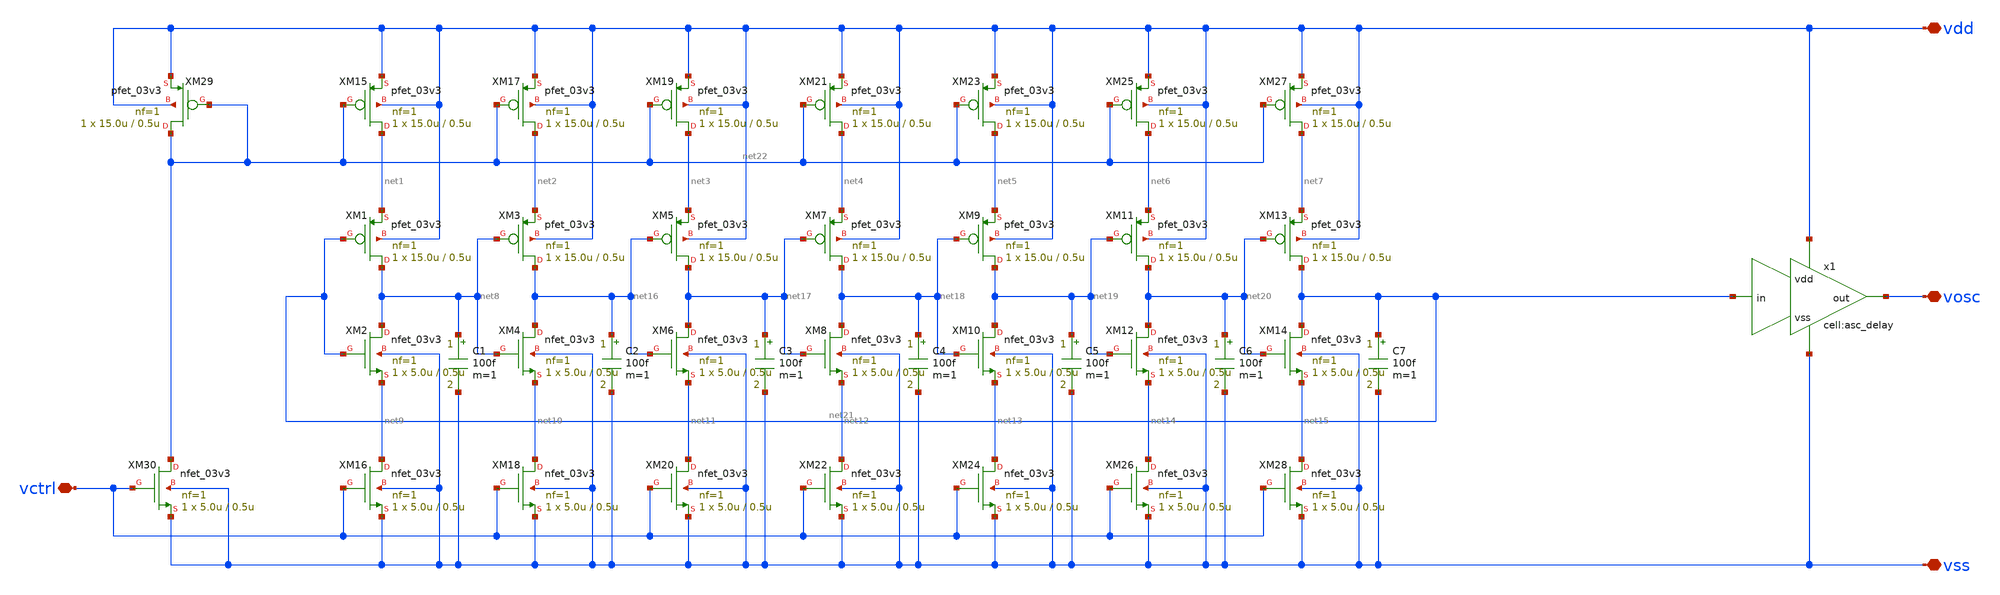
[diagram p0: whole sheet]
** sch_path: designs/libs/core_analog/CSRVCO_20250821/CSRVCO_20250821.sch
**.subckt CSRVCO_20250821 vdd vss vosc vctrl
*.iopin vdd
*.iopin vss
*.iopin vosc
*.iopin vctrl
XM1 net8 net21 net1 vdd pfet_03v3 L=0.5u W=15.0u nf=1 ad='int((nf+1)/2) * W/nf * 0.18u' as='int((nf+2)/2) * W/nf * 0.18u'
+ pd='2*int((nf+1)/2) * (W/nf + 0.18u)' ps='2*int((nf+2)/2) * (W/nf + 0.18u)' nrd='0.18u / W' nrs='0.18u / W'
+ sa=0 sb=0 sd=0 m=1
XM2 net8 net21 net9 vss nfet_03v3 L=0.5u W=5.0u nf=1 ad='int((nf+1)/2) * W/nf * 0.18u' as='int((nf+2)/2) * W/nf * 0.18u'
+ pd='2*int((nf+1)/2) * (W/nf + 0.18u)' ps='2*int((nf+2)/2) * (W/nf + 0.18u)' nrd='0.18u / W' nrs='0.18u / W'
+ sa=0 sb=0 sd=0 m=1
XM3 net16 net8 net2 vdd pfet_03v3 L=0.5u W=15.0u nf=1 ad='int((nf+1)/2) * W/nf * 0.18u' as='int((nf+2)/2) * W/nf * 0.18u'
+ pd='2*int((nf+1)/2) * (W/nf + 0.18u)' ps='2*int((nf+2)/2) * (W/nf + 0.18u)' nrd='0.18u / W' nrs='0.18u / W'
+ sa=0 sb=0 sd=0 m=1
XM4 net16 net8 net10 vss nfet_03v3 L=0.5u W=5.0u nf=1 ad='int((nf+1)/2) * W/nf * 0.18u' as='int((nf+2)/2) * W/nf * 0.18u'
+ pd='2*int((nf+1)/2) * (W/nf + 0.18u)' ps='2*int((nf+2)/2) * (W/nf + 0.18u)' nrd='0.18u / W' nrs='0.18u / W'
+ sa=0 sb=0 sd=0 m=1
XM5 net17 net16 net3 vdd pfet_03v3 L=0.5u W=15.0u nf=1 ad='int((nf+1)/2) * W/nf * 0.18u' as='int((nf+2)/2) * W/nf * 0.18u'
+ pd='2*int((nf+1)/2) * (W/nf + 0.18u)' ps='2*int((nf+2)/2) * (W/nf + 0.18u)' nrd='0.18u / W' nrs='0.18u / W'
+ sa=0 sb=0 sd=0 m=1
XM6 net17 net16 net11 vss nfet_03v3 L=0.5u W=5.0u nf=1 ad='int((nf+1)/2) * W/nf * 0.18u' as='int((nf+2)/2) * W/nf * 0.18u'
+ pd='2*int((nf+1)/2) * (W/nf + 0.18u)' ps='2*int((nf+2)/2) * (W/nf + 0.18u)' nrd='0.18u / W' nrs='0.18u / W'
+ sa=0 sb=0 sd=0 m=1
XM7 net18 net17 net4 vdd pfet_03v3 L=0.5u W=15.0u nf=1 ad='int((nf+1)/2) * W/nf * 0.18u' as='int((nf+2)/2) * W/nf * 0.18u'
+ pd='2*int((nf+1)/2) * (W/nf + 0.18u)' ps='2*int((nf+2)/2) * (W/nf + 0.18u)' nrd='0.18u / W' nrs='0.18u / W'
+ sa=0 sb=0 sd=0 m=1
XM8 net18 net17 net12 vss nfet_03v3 L=0.5u W=5.0u nf=1 ad='int((nf+1)/2) * W/nf * 0.18u' as='int((nf+2)/2) * W/nf * 0.18u'
+ pd='2*int((nf+1)/2) * (W/nf + 0.18u)' ps='2*int((nf+2)/2) * (W/nf + 0.18u)' nrd='0.18u / W' nrs='0.18u / W'
+ sa=0 sb=0 sd=0 m=1
XM9 net19 net18 net5 vdd pfet_03v3 L=0.5u W=15.0u nf=1 ad='int((nf+1)/2) * W/nf * 0.18u' as='int((nf+2)/2) * W/nf * 0.18u'
+ pd='2*int((nf+1)/2) * (W/nf + 0.18u)' ps='2*int((nf+2)/2) * (W/nf + 0.18u)' nrd='0.18u / W' nrs='0.18u / W'
+ sa=0 sb=0 sd=0 m=1
XM10 net19 net18 net13 vss nfet_03v3 L=0.5u W=5.0u nf=1 ad='int((nf+1)/2) * W/nf * 0.18u' as='int((nf+2)/2) * W/nf * 0.18u'
+ pd='2*int((nf+1)/2) * (W/nf + 0.18u)' ps='2*int((nf+2)/2) * (W/nf + 0.18u)' nrd='0.18u / W' nrs='0.18u / W'
+ sa=0 sb=0 sd=0 m=1
XM11 net20 net19 net6 vdd pfet_03v3 L=0.5u W=15.0u nf=1 ad='int((nf+1)/2) * W/nf * 0.18u' as='int((nf+2)/2) * W/nf * 0.18u'
+ pd='2*int((nf+1)/2) * (W/nf + 0.18u)' ps='2*int((nf+2)/2) * (W/nf + 0.18u)' nrd='0.18u / W' nrs='0.18u / W'
+ sa=0 sb=0 sd=0 m=1
XM12 net20 net19 net14 vss nfet_03v3 L=0.5u W=5.0u nf=1 ad='int((nf+1)/2) * W/nf * 0.18u' as='int((nf+2)/2) * W/nf * 0.18u'
+ pd='2*int((nf+1)/2) * (W/nf + 0.18u)' ps='2*int((nf+2)/2) * (W/nf + 0.18u)' nrd='0.18u / W' nrs='0.18u / W'
+ sa=0 sb=0 sd=0 m=1
XM13 net21 net20 net7 vdd pfet_03v3 L=0.5u W=15.0u nf=1 ad='int((nf+1)/2) * W/nf * 0.18u' as='int((nf+2)/2) * W/nf * 0.18u'
+ pd='2*int((nf+1)/2) * (W/nf + 0.18u)' ps='2*int((nf+2)/2) * (W/nf + 0.18u)' nrd='0.18u / W' nrs='0.18u / W'
+ sa=0 sb=0 sd=0 m=1
XM14 net21 net20 net15 vss nfet_03v3 L=0.5u W=5.0u nf=1 ad='int((nf+1)/2) * W/nf * 0.18u' as='int((nf+2)/2) * W/nf * 0.18u'
+ pd='2*int((nf+1)/2) * (W/nf + 0.18u)' ps='2*int((nf+2)/2) * (W/nf + 0.18u)' nrd='0.18u / W' nrs='0.18u / W'
+ sa=0 sb=0 sd=0 m=1
XM15 net1 net22 vdd vdd pfet_03v3 L=0.5u W=15.0u nf=1 ad='int((nf+1)/2) * W/nf * 0.18u' as='int((nf+2)/2) * W/nf * 0.18u'
+ pd='2*int((nf+1)/2) * (W/nf + 0.18u)' ps='2*int((nf+2)/2) * (W/nf + 0.18u)' nrd='0.18u / W' nrs='0.18u / W'
+ sa=0 sb=0 sd=0 m=1
XM16 net9 vctrl vss vss nfet_03v3 L=0.5u W=5.0u nf=1 ad='int((nf+1)/2) * W/nf * 0.18u' as='int((nf+2)/2) * W/nf * 0.18u'
+ pd='2*int((nf+1)/2) * (W/nf + 0.18u)' ps='2*int((nf+2)/2) * (W/nf + 0.18u)' nrd='0.18u / W' nrs='0.18u / W'
+ sa=0 sb=0 sd=0 m=1
XM17 net2 net22 vdd vdd pfet_03v3 L=0.5u W=15.0u nf=1 ad='int((nf+1)/2) * W/nf * 0.18u' as='int((nf+2)/2) * W/nf * 0.18u'
+ pd='2*int((nf+1)/2) * (W/nf + 0.18u)' ps='2*int((nf+2)/2) * (W/nf + 0.18u)' nrd='0.18u / W' nrs='0.18u / W'
+ sa=0 sb=0 sd=0 m=1
XM18 net10 vctrl vss vss nfet_03v3 L=0.5u W=5.0u nf=1 ad='int((nf+1)/2) * W/nf * 0.18u' as='int((nf+2)/2) * W/nf * 0.18u'
+ pd='2*int((nf+1)/2) * (W/nf + 0.18u)' ps='2*int((nf+2)/2) * (W/nf + 0.18u)' nrd='0.18u / W' nrs='0.18u / W'
+ sa=0 sb=0 sd=0 m=1
XM19 net3 net22 vdd vdd pfet_03v3 L=0.5u W=15.0u nf=1 ad='int((nf+1)/2) * W/nf * 0.18u' as='int((nf+2)/2) * W/nf * 0.18u'
+ pd='2*int((nf+1)/2) * (W/nf + 0.18u)' ps='2*int((nf+2)/2) * (W/nf + 0.18u)' nrd='0.18u / W' nrs='0.18u / W'
+ sa=0 sb=0 sd=0 m=1
XM20 net11 vctrl vss vss nfet_03v3 L=0.5u W=5.0u nf=1 ad='int((nf+1)/2) * W/nf * 0.18u' as='int((nf+2)/2) * W/nf * 0.18u'
+ pd='2*int((nf+1)/2) * (W/nf + 0.18u)' ps='2*int((nf+2)/2) * (W/nf + 0.18u)' nrd='0.18u / W' nrs='0.18u / W'
+ sa=0 sb=0 sd=0 m=1
XM21 net4 net22 vdd vdd pfet_03v3 L=0.5u W=15.0u nf=1 ad='int((nf+1)/2) * W/nf * 0.18u' as='int((nf+2)/2) * W/nf * 0.18u'
+ pd='2*int((nf+1)/2) * (W/nf + 0.18u)' ps='2*int((nf+2)/2) * (W/nf + 0.18u)' nrd='0.18u / W' nrs='0.18u / W'
+ sa=0 sb=0 sd=0 m=1
XM22 net12 vctrl vss vss nfet_03v3 L=0.5u W=5.0u nf=1 ad='int((nf+1)/2) * W/nf * 0.18u' as='int((nf+2)/2) * W/nf * 0.18u'
+ pd='2*int((nf+1)/2) * (W/nf + 0.18u)' ps='2*int((nf+2)/2) * (W/nf + 0.18u)' nrd='0.18u / W' nrs='0.18u / W'
+ sa=0 sb=0 sd=0 m=1
XM23 net5 net22 vdd vdd pfet_03v3 L=0.5u W=15.0u nf=1 ad='int((nf+1)/2) * W/nf * 0.18u' as='int((nf+2)/2) * W/nf * 0.18u'
+ pd='2*int((nf+1)/2) * (W/nf + 0.18u)' ps='2*int((nf+2)/2) * (W/nf + 0.18u)' nrd='0.18u / W' nrs='0.18u / W'
+ sa=0 sb=0 sd=0 m=1
XM24 net13 vctrl vss vss nfet_03v3 L=0.5u W=5.0u nf=1 ad='int((nf+1)/2) * W/nf * 0.18u' as='int((nf+2)/2) * W/nf * 0.18u'
+ pd='2*int((nf+1)/2) * (W/nf + 0.18u)' ps='2*int((nf+2)/2) * (W/nf + 0.18u)' nrd='0.18u / W' nrs='0.18u / W'
+ sa=0 sb=0 sd=0 m=1
XM25 net6 net22 vdd vdd pfet_03v3 L=0.5u W=15.0u nf=1 ad='int((nf+1)/2) * W/nf * 0.18u' as='int((nf+2)/2) * W/nf * 0.18u'
+ pd='2*int((nf+1)/2) * (W/nf + 0.18u)' ps='2*int((nf+2)/2) * (W/nf + 0.18u)' nrd='0.18u / W' nrs='0.18u / W'
+ sa=0 sb=0 sd=0 m=1
XM26 net14 vctrl vss vss nfet_03v3 L=0.5u W=5.0u nf=1 ad='int((nf+1)/2) * W/nf * 0.18u' as='int((nf+2)/2) * W/nf * 0.18u'
+ pd='2*int((nf+1)/2) * (W/nf + 0.18u)' ps='2*int((nf+2)/2) * (W/nf + 0.18u)' nrd='0.18u / W' nrs='0.18u / W'
+ sa=0 sb=0 sd=0 m=1
XM27 net7 net22 vdd vdd pfet_03v3 L=0.5u W=15.0u nf=1 ad='int((nf+1)/2) * W/nf * 0.18u' as='int((nf+2)/2) * W/nf * 0.18u'
+ pd='2*int((nf+1)/2) * (W/nf + 0.18u)' ps='2*int((nf+2)/2) * (W/nf + 0.18u)' nrd='0.18u / W' nrs='0.18u / W'
+ sa=0 sb=0 sd=0 m=1
XM28 net15 vctrl vss vss nfet_03v3 L=0.5u W=5.0u nf=1 ad='int((nf+1)/2) * W/nf * 0.18u' as='int((nf+2)/2) * W/nf * 0.18u'
+ pd='2*int((nf+1)/2) * (W/nf + 0.18u)' ps='2*int((nf+2)/2) * (W/nf + 0.18u)' nrd='0.18u / W' nrs='0.18u / W'
+ sa=0 sb=0 sd=0 m=1
XM29 net22 net22 vdd vdd pfet_03v3 L=0.5u W=15.0u nf=1 ad='int((nf+1)/2) * W/nf * 0.18u' as='int((nf+2)/2) * W/nf * 0.18u'
+ pd='2*int((nf+1)/2) * (W/nf + 0.18u)' ps='2*int((nf+2)/2) * (W/nf + 0.18u)' nrd='0.18u / W' nrs='0.18u / W'
+ sa=0 sb=0 sd=0 m=1
XM30 net22 vctrl vss vss nfet_03v3 L=0.5u W=5.0u nf=1 ad='int((nf+1)/2) * W/nf * 0.18u' as='int((nf+2)/2) * W/nf * 0.18u'
+ pd='2*int((nf+1)/2) * (W/nf + 0.18u)' ps='2*int((nf+2)/2) * (W/nf + 0.18u)' nrd='0.18u / W' nrs='0.18u / W'
+ sa=0 sb=0 sd=0 m=1
x1 net21 vss vosc vdd asc_delay
C1 net8 vss 100f m=1
C2 net16 vss 100f m=1
C3 net17 vss 100f m=1
C4 net18 vss 100f m=1
C5 net19 vss 100f m=1
C6 net20 vss 100f m=1
C7 net21 vss 100f m=1
**.ends
.end
